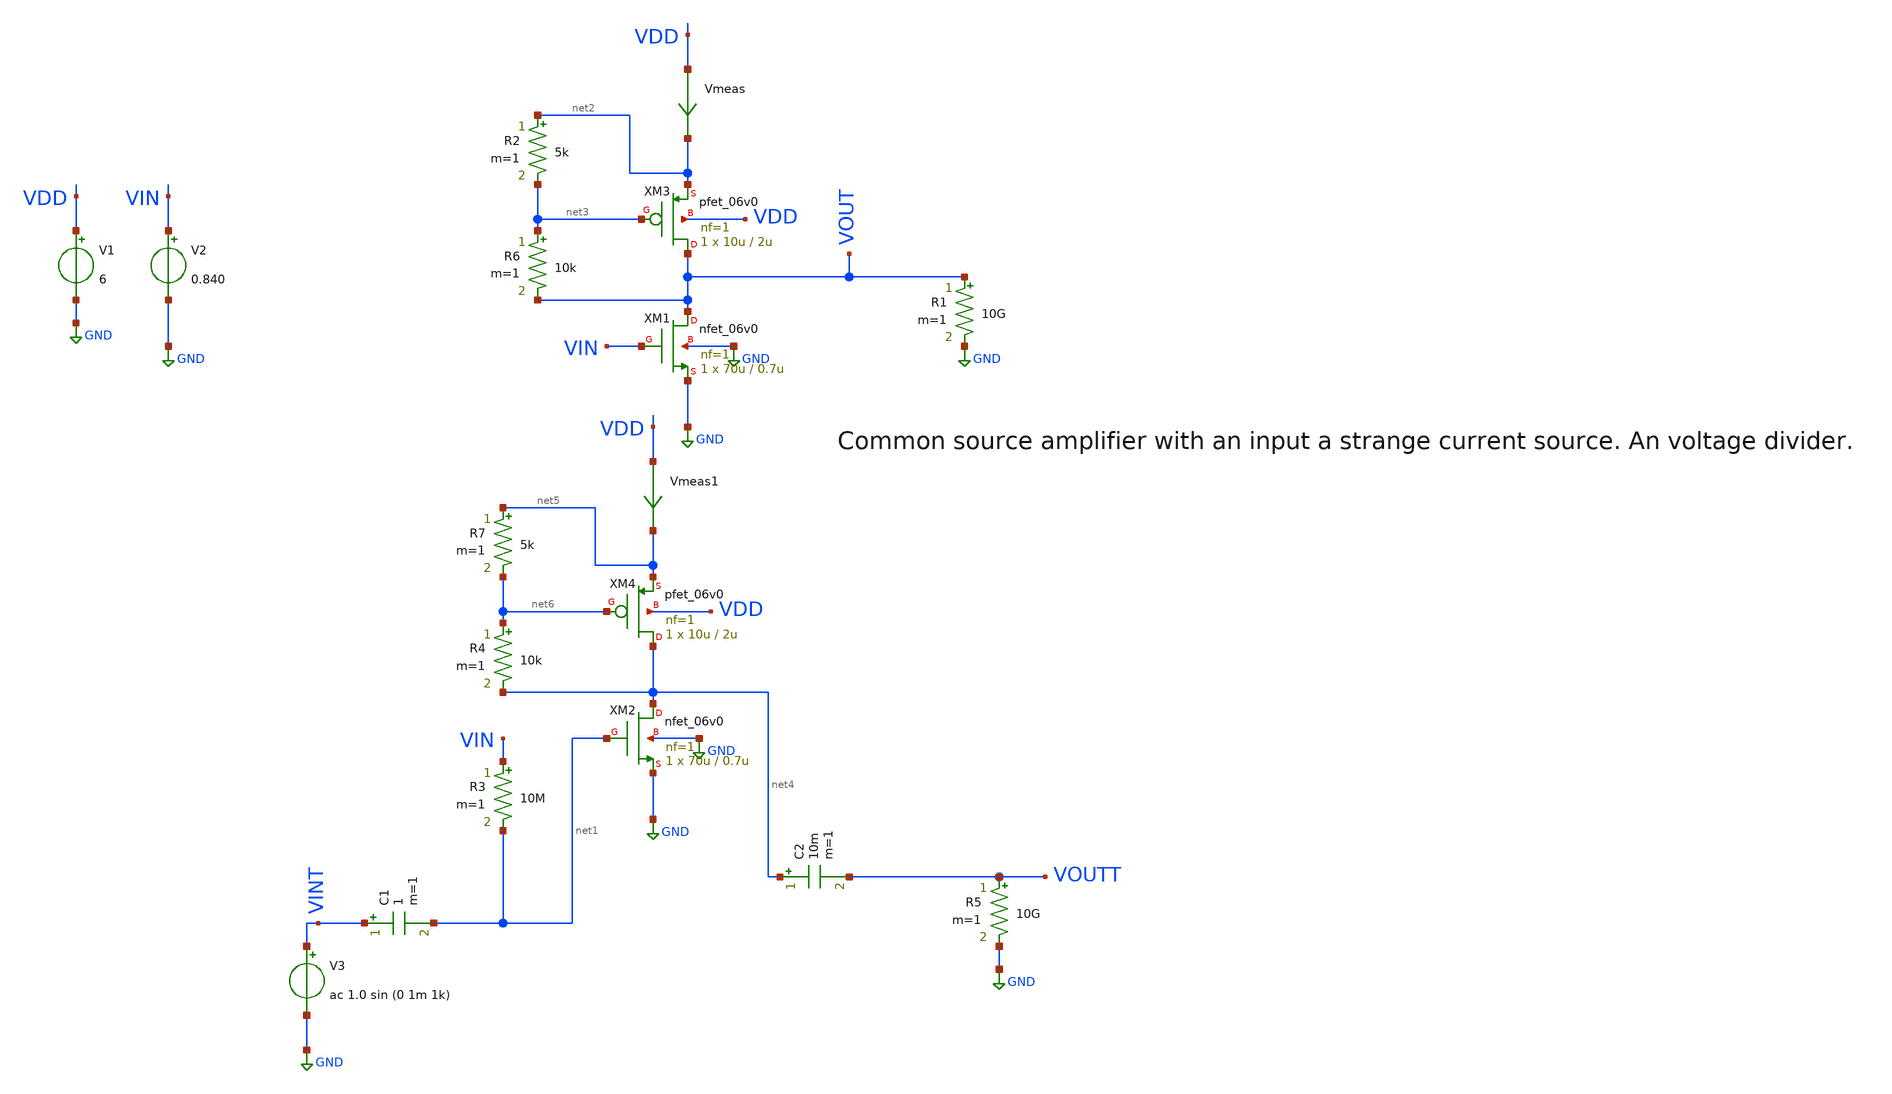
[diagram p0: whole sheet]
** sch_path: unusual_amplifiers/unusual_amp8.sch
**.subckt unusual_amp8
Vmeas VDD net2 0
.save i(vmeas)
V1 VDD GND 6
V2 VIN GND 0.840
V3 VINT GND ac 1.0 sin (0 1m 1k)
R3 VIN net1 10M m=1
R5 VOUTT GND 10G m=1
R1 VOUT GND 10G m=1
C1 VINT net1 1 m=1
XM1 VOUT VIN GND GND nfet_06v0 L=0.7u W=70u nf=1 ad='int((nf+1)/2) * W/nf * 0.18u' as='int((nf+2)/2) * W/nf * 0.18u'
+ pd='2*int((nf+1)/2) * (W/nf + 0.18u)' ps='2*int((nf+2)/2) * (W/nf + 0.18u)' nrd='0.18u / W' nrs='0.18u / W'
+ sa=0 sb=0 sd=0 m=1
R2 net2 net3 5k m=1
XM3 VOUT net3 net2 VDD pfet_06v0 L=2u W=10u nf=1 ad='int((nf+1)/2) * W/nf * 0.18u' as='int((nf+2)/2) * W/nf * 0.18u'
+ pd='2*int((nf+1)/2) * (W/nf + 0.18u)' ps='2*int((nf+2)/2) * (W/nf + 0.18u)' nrd='0.18u / W' nrs='0.18u / W'
+ sa=0 sb=0 sd=0 m=1
C2 net4 VOUTT 10m m=1
R6 net3 VOUT 10k m=1
Vmeas1 VDD net5 0
.save i(vmeas1)
XM2 net4 net1 GND GND nfet_06v0 L=0.7u W=70u nf=1 ad='int((nf+1)/2) * W/nf * 0.18u' as='int((nf+2)/2) * W/nf * 0.18u'
+ pd='2*int((nf+1)/2) * (W/nf + 0.18u)' ps='2*int((nf+2)/2) * (W/nf + 0.18u)' nrd='0.18u / W' nrs='0.18u / W'
+ sa=0 sb=0 sd=0 m=1
XM4 net4 net6 net5 VDD pfet_06v0 L=2u W=10u nf=1 ad='int((nf+1)/2) * W/nf * 0.18u' as='int((nf+2)/2) * W/nf * 0.18u'
+ pd='2*int((nf+1)/2) * (W/nf + 0.18u)' ps='2*int((nf+2)/2) * (W/nf + 0.18u)' nrd='0.18u / W' nrs='0.18u / W'
+ sa=0 sb=0 sd=0 m=1
R4 net6 net4 10k m=1
R7 net5 net6 5k m=1
**** begin user architecture code

**************************************************************
**************************************************************
**************************************************************
**************************************************************
**************************************************************
*LIBs*********************************************************
**************************************************************
**************************************************************
**************************************************************
**************************************************************
**************************************************************
.include $::180MCU_MODELS/design.ngspice
*.lib $::180MCU_MODELS/sm141064.ngspice statistical *use statistical if you want global and parameter mismatch
*.lib $::180MCU_MODELS/sm141064.ngspice res_statistical
.lib $::180MCU_MODELS/sm141064.ngspice typical
.lib $::180MCU_MODELS/sm141064.ngspice res_typical
.lib $::180MCU_MODELS/sm141064.ngspice moscap_typical
.lib $::180MCU_MODELS/sm141064.ngspice bjt_typical
.lib $::180MCU_MODELS/sm141064.ngspice diode_typical
.lib $::180MCU_MODELS/sm141064.ngspice mimcap_typical
**************************************************************
**************************************************************
**************************************************************
**************************************************************
**************************************************************
*Corners/montecarlo options***********************************
**************************************************************
**************************************************************
**************************************************************
**************************************************************
**************************************************************
.TEMP 27
.param   sw_stat_global = 1   sw_stat_mism = 1  mc_skew = 3  res_mc_skew = 3  cap_mc_skew = 3
+  fnoicor = 1
**************************************************************
**************************************************************
**************************************************************
**************************************************************
*SIMULATION and Plots*****************************************
**************************************************************
**************************************************************
**************************************************************
**************************************************************
.control
save all
dc V2 0 6 0.01
*dc simulation
plot v(VOUT) v(VIN) deriv(v(VOUT))
*ploting VIN VOUT and the voltage gain
plot i(Vmeas)
*ploting the current for curiosity
tran 100ns 2m
*transient simulation
plot (v(VINT)) (v(VOUTT))
*simple plot to exemplify the gain
fft v(VOUTT) v(VINT)
*fast fourier transfor
plot mag(v(VOUTT)) mag(v(VINT))
* analyse the frequency spectrum of the transient waves, to detect distortion
ac dec 20 1 50G
*simple ac simulation
plot v(VOUTT)
*gain in function of the input frequency
.endc

**** end user architecture code
**.ends
.GLOBAL GND
.end
